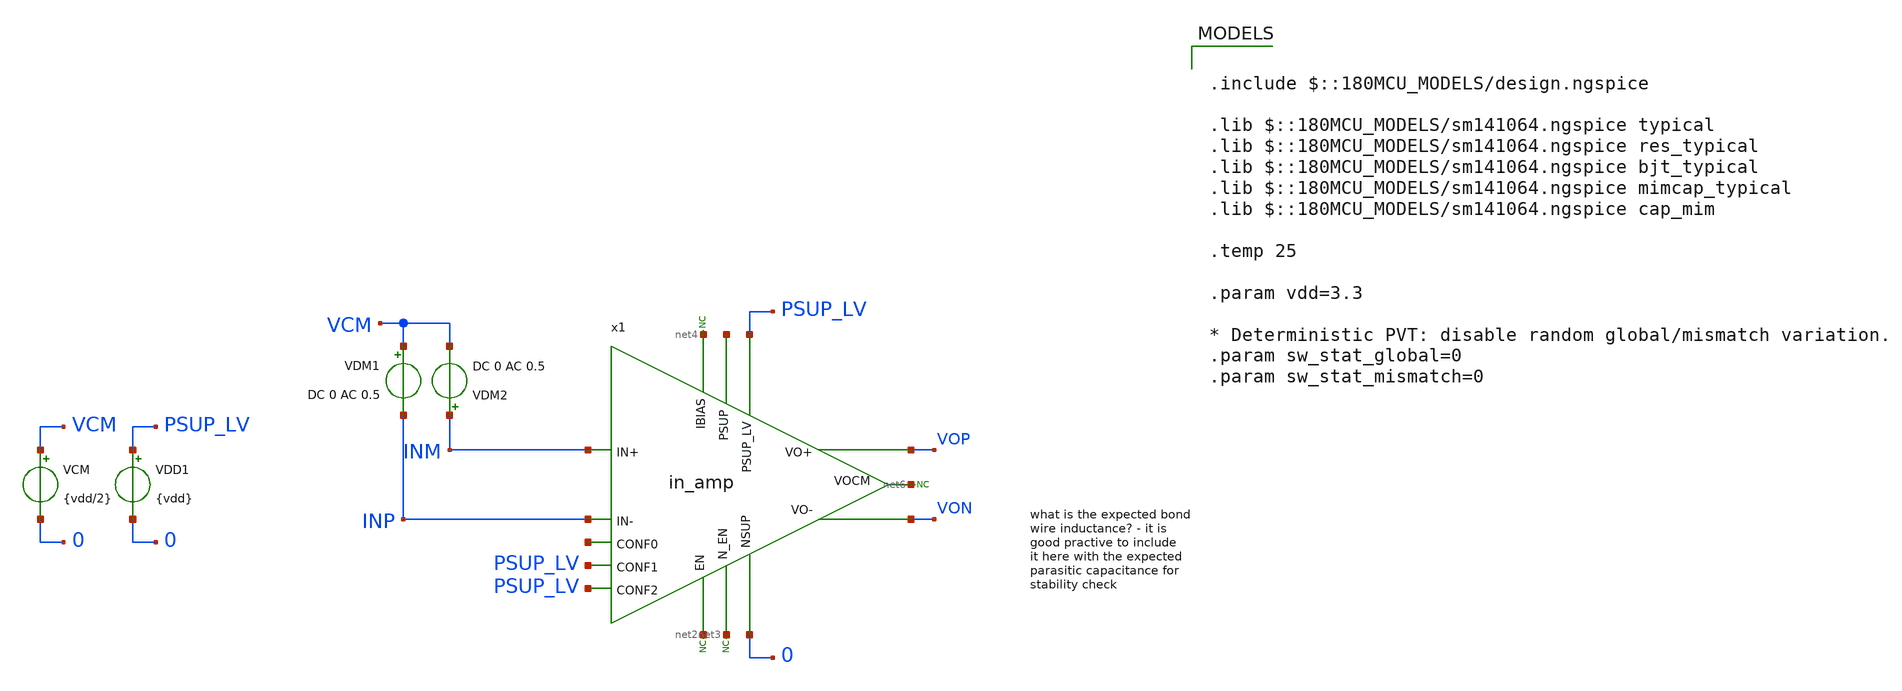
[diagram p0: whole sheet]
** sch_path: xschem/blocks/INA/tb_INA_gain.sch
**.subckt tb_INA_gain
x1 net1 PSUP_LV 0 net2 net3 net4 net5 PSUP_LV PSUP_LV INM VOP net6 INP VON in_amp
VDD1 PSUP_LV 0 {vdd}
VCM VCM 0 {vdd/2}
* noconn #net6
* noconn #net4
* noconn #net2
* noconn #net3
VDM2 INM VCM DC 0 AC 0.5
VDM1 VCM INP DC 0 AC 0.5
**** begin user architecture code

.include $::180MCU_MODELS/design.ngspice

.lib $::180MCU_MODELS/sm141064.ngspice typical
.lib $::180MCU_MODELS/sm141064.ngspice res_typical
.lib $::180MCU_MODELS/sm141064.ngspice bjt_typical
.lib $::180MCU_MODELS/sm141064.ngspice mimcap_typical
.lib $::180MCU_MODELS/sm141064.ngspice cap_mim

.temp 25

.param vdd=3.3

* Deterministic PVT: disable random global/mismatch variation.
.param sw_stat_global=0
.param sw_stat_mismatch=0



.control
set units=degrees
save all
ac dec 100 1 1G

let Vid = v(INP) - v(INM)
let Vo = v(Vop) - v(Von)
let aol = v(Vo) / v(Vid)
let gain_db = db(aol)
let phase_deg = cph(aol)

*write tb_in_amp_gain.raw frequency v(Vop) v(Von) v(Vo) aol gain_db phase_deg
write tb_in_amp_gain.raw

.endc


**** end user architecture code
**.ends

* expanding   symbol:  blocks/in_amp/in_amp.sym # of pins=14
** sym_path: xschem/blocks/in_amp/in_amp.sym
** sch_path: xschem/blocks/in_amp/in_amp.sch
.subckt in_amp PSUP PSUP_LV NSUP EN N_EN IBIAS CONF0 CONF1 CONF2 IN+ VO+ VOCM IN- VO-
*.opin VO+
*.opin VO-
*.ipin IN+
*.ipin IN-
*.ipin PSUP
*.ipin NSUP
*.ipin EN
*.ipin N_EN
*.ipin IBIAS
*.ipin PSUP_LV
*.ipin CONF0
*.ipin CONF1
*.ipin CONF2
*.opin VOCM
x1 PSUP net1 IN- net2 IN+ VO+ VO- IBIAS N_EN EN NSUP fdda
.ends


* expanding   symbol:  blocks/fdda/fdda.sym # of pins=11
** sym_path: xschem/blocks/fdda/fdda.sym
** sch_path: xschem/blocks/fdda/fdda.sch
.subckt fdda PSUP Vp- Vn+ Vn- Vp+ Vo+ Vo- IBIAS N_EN EN NSUP
*.ipin PSUP
*.ipin NSUP
*.ipin N_EN
*.ipin EN
*.ipin IBIAS
*.ipin Vp+
*.ipin Vp-
*.ipin Vn+
*.ipin Vn-
*.opin Vo+
*.opin Vo-
* noconn N_EN
* noconn EN
I0 net5 NSUP 1u
XM9 Vo+ Vp- net1 NSUP pfet_06v0 L=2u W=4u nf=5 ad='int((nf+1)/2) * W/nf * 0.18u' as='int((nf+2)/2) * W/nf * 0.18u'
+ pd='2*int((nf+1)/2) * (W/nf + 0.18u)' ps='2*int((nf+2)/2) * (W/nf + 0.18u)' nrd='0.18u / W' nrs='0.18u / W'
+ sa=0 sb=0 sd=0 m=10
XM1 Vo- Vp+ net1 NSUP pfet_06v0 L=2u W=4u nf=5 ad='int((nf+1)/2) * W/nf * 0.18u' as='int((nf+2)/2) * W/nf * 0.18u'
+ pd='2*int((nf+1)/2) * (W/nf + 0.18u)' ps='2*int((nf+2)/2) * (W/nf + 0.18u)' nrd='0.18u / W' nrs='0.18u / W'
+ sa=0 sb=0 sd=0 m=10
XM2 net1 vb1 PSUP net3 pfet_06v0 L=4u W=2u nf=1 ad='int((nf+1)/2) * W/nf * 0.18u' as='int((nf+2)/2) * W/nf * 0.18u'
+ pd='2*int((nf+1)/2) * (W/nf + 0.18u)' ps='2*int((nf+2)/2) * (W/nf + 0.18u)' nrd='0.18u / W' nrs='0.18u / W'
+ sa=0 sb=0 sd=0 m=8
XM3 Vo- Vo- NSUP NSUP nfet_06v0 L=4u W=2u nf=1 ad='int((nf+1)/2) * W/nf * 0.18u' as='int((nf+2)/2) * W/nf * 0.18u'
+ pd='2*int((nf+1)/2) * (W/nf + 0.18u)' ps='2*int((nf+2)/2) * (W/nf + 0.18u)' nrd='0.18u / W' nrs='0.18u / W'
+ sa=0 sb=0 sd=0 m=4
XM4 Vo+ Vn- net2 NSUP pfet_06v0 L=2u W=4u nf=5 ad='int((nf+1)/2) * W/nf * 0.18u' as='int((nf+2)/2) * W/nf * 0.18u'
+ pd='2*int((nf+1)/2) * (W/nf + 0.18u)' ps='2*int((nf+2)/2) * (W/nf + 0.18u)' nrd='0.18u / W' nrs='0.18u / W'
+ sa=0 sb=0 sd=0 m=10
XM5 Vo- Vn+ net2 NSUP pfet_06v0 L=2u W=4u nf=5 ad='int((nf+1)/2) * W/nf * 0.18u' as='int((nf+2)/2) * W/nf * 0.18u'
+ pd='2*int((nf+1)/2) * (W/nf + 0.18u)' ps='2*int((nf+2)/2) * (W/nf + 0.18u)' nrd='0.18u / W' nrs='0.18u / W'
+ sa=0 sb=0 sd=0 m=10
XM6 net2 vb1 PSUP PSUP pfet_06v0 L=4u W=2u nf=1 ad='int((nf+1)/2) * W/nf * 0.18u' as='int((nf+2)/2) * W/nf * 0.18u'
+ pd='2*int((nf+1)/2) * (W/nf + 0.18u)' ps='2*int((nf+2)/2) * (W/nf + 0.18u)' nrd='0.18u / W' nrs='0.18u / W'
+ sa=0 sb=0 sd=0 m=8
XM8 Vo+ Vo+ NSUP NSUP nfet_06v0 L=4u W=2u nf=1 ad='int((nf+1)/2) * W/nf * 0.18u' as='int((nf+2)/2) * W/nf * 0.18u'
+ pd='2*int((nf+1)/2) * (W/nf + 0.18u)' ps='2*int((nf+2)/2) * (W/nf + 0.18u)' nrd='0.18u / W' nrs='0.18u / W'
+ sa=0 sb=0 sd=0 m=4
XM7 net5 vb1 PSUP net4 pfet_06v0 L=4u W=2u nf=1 ad='int((nf+1)/2) * W/nf * 0.18u' as='int((nf+2)/2) * W/nf * 0.18u'
+ pd='2*int((nf+1)/2) * (W/nf + 0.18u)' ps='2*int((nf+2)/2) * (W/nf + 0.18u)' nrd='0.18u / W' nrs='0.18u / W'
+ sa=0 sb=0 sd=0 m=4
.ends

.end
